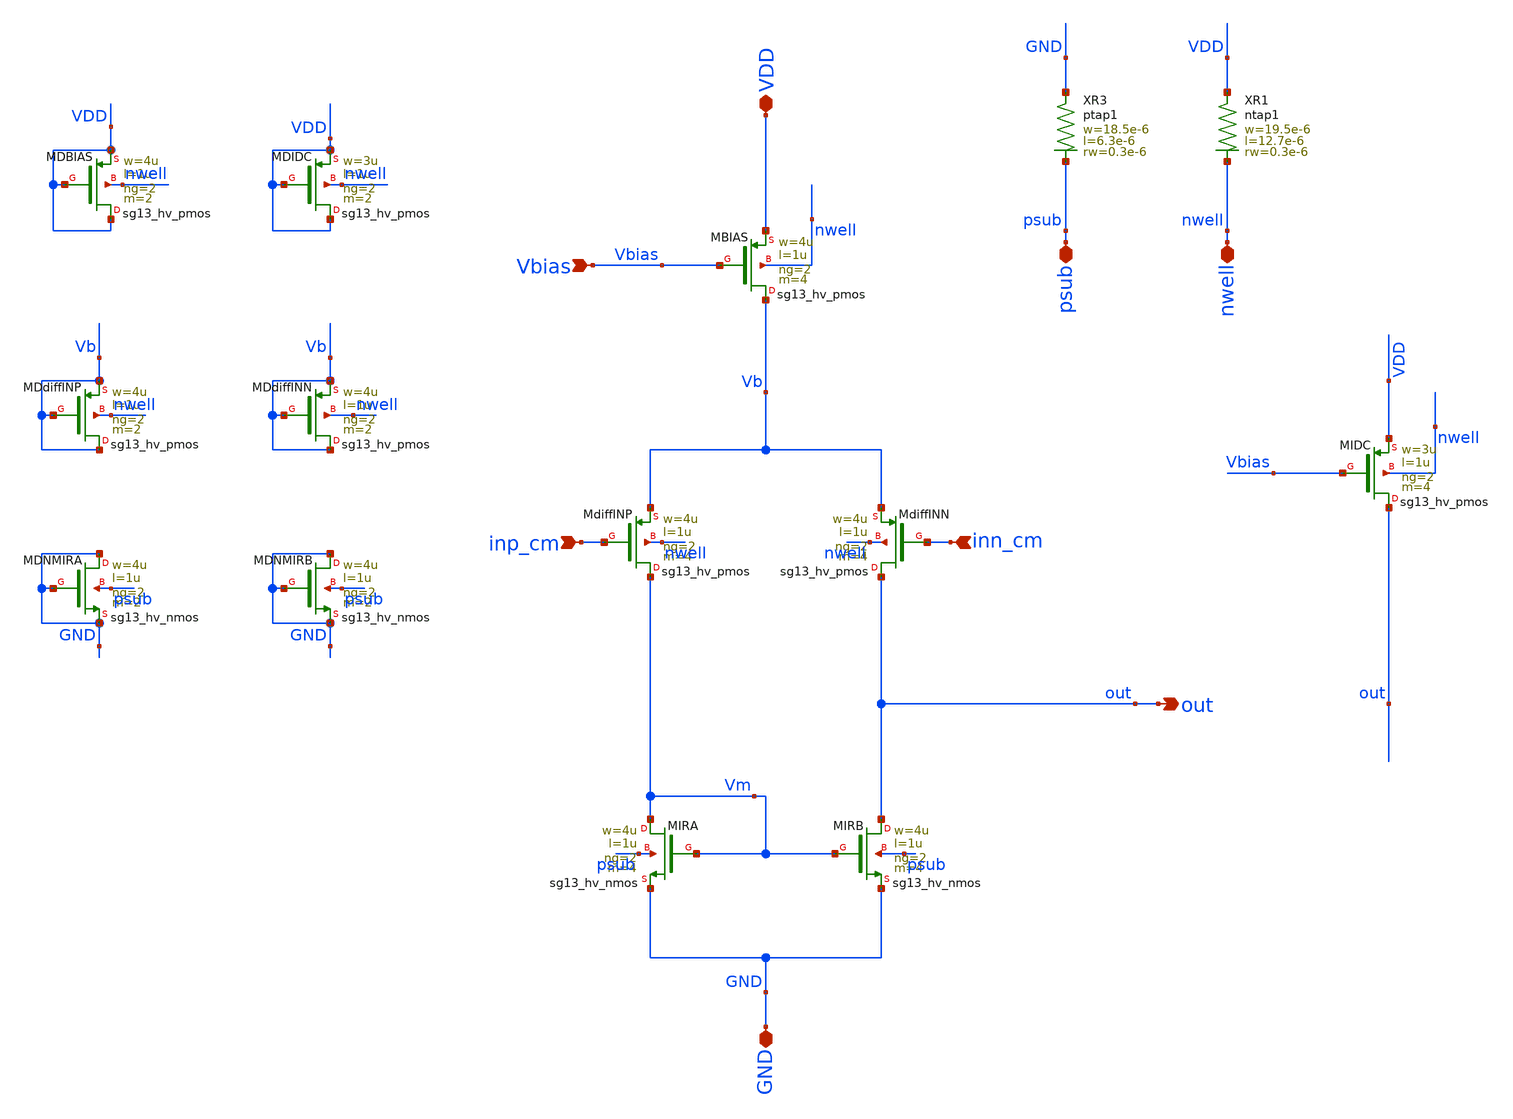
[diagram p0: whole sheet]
** sch_path: xschem/V2I_shift_final.sch
**.subckt V2I_shift_final inn_cm inp_cm out Vbias VDD GND psub nwell
*.ipin inn_cm
*.ipin inp_cm
*.opin out
*.ipin Vbias
*.iopin VDD
*.iopin GND
*.iopin psub
*.iopin nwell
XMIRA Vm Vm GND psub sg13_hv_nmos w=4u l=1u ng=2 m=4 mm_ok=1
XMBIAS Vb Vbias VDD nwell sg13_hv_pmos w=4u l=1u ng=2 m=4 mm_ok=1
XMIRB out Vm GND psub sg13_hv_nmos w=4u l=1u ng=2 m=4 mm_ok=1
XMdiffINN out inn_cm Vb nwell sg13_hv_pmos w=4u l=1u ng=2 m=4 mm_ok=1
XMDBIAS VDD VDD VDD nwell sg13_hv_pmos w=4u l=1u ng=2 m=2 mm_ok=1
XMIDC out Vbias VDD nwell sg13_hv_pmos w=3u l=1u ng=2 m=4 mm_ok=1
XMDIDC VDD VDD VDD nwell sg13_hv_pmos w=3u l=1u ng=2 m=2 mm_ok=1
XMdiffINP Vm inp_cm Vb nwell sg13_hv_pmos w=4u l=1u ng=2 m=4 mm_ok=1
XMDdiffINP Vb Vb Vb nwell sg13_hv_pmos w=4u l=1u ng=2 m=2 mm_ok=1
XMDdiffINN Vb Vb Vb nwell sg13_hv_pmos w=4u l=1u ng=2 m=2 mm_ok=1
XMDNMIRA GND GND GND psub sg13_hv_nmos w=4u l=1u ng=2 m=2 mm_ok=1
XMDNMIRB GND GND GND psub sg13_hv_nmos w=4u l=1u ng=2 m=2 mm_ok=1
XR3 GND psub ptap1 R=4.709 w=18.5e-6 l=6.3e-6 rw=0.3e-6
XR1 VDD nwell ntap1 R=3.606 w=19.5e-6 l=12.7e-6 rw=0.3e-6
**.ends
.end
